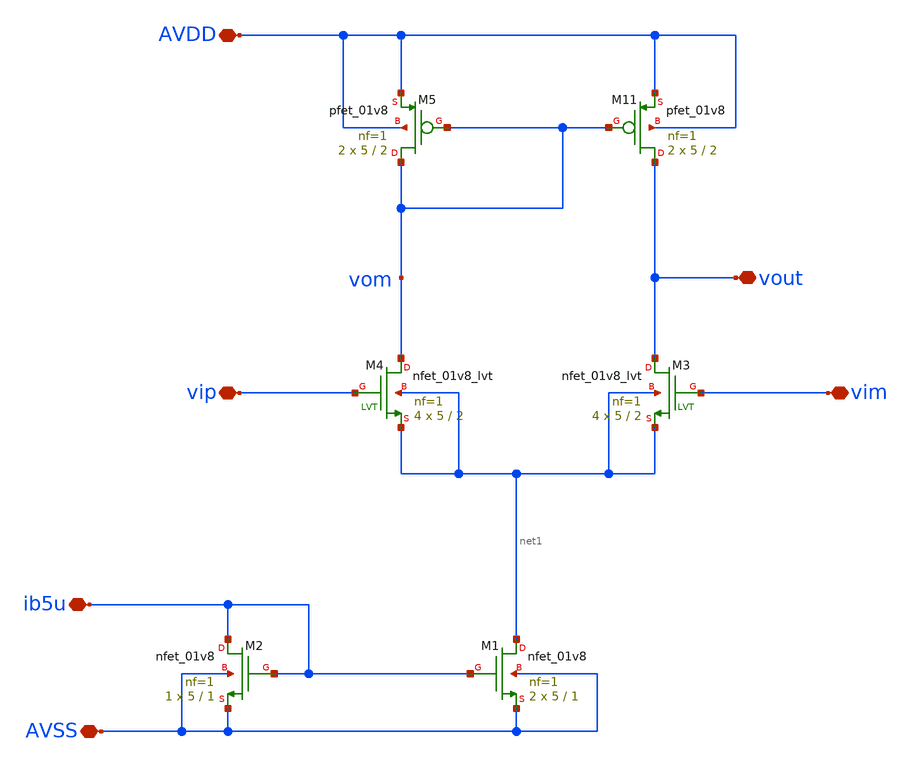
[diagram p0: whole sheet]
** sch_path: xschem/Opa_nmos1.sch
**.subckt Opa_nmos1 vip vim AVDD AVSS vout ib5u
*.iopin vip
*.iopin vim
*.iopin AVDD
*.iopin AVSS
*.iopin vout
*.iopin ib5u
XM4 vom vip net1 net1 sky130_fd_pr__nfet_01v8_lvt L=2 W=5 nf=1 ad='int((1 + 1)/2) * 5 / 1 * 0.29' as='int((1 + 2)/2) * 5 / 1 * 0.29'
+ pd='2*int((1 + 1)/2) * (5 / 1 + 0.29)' ps='2*int((1 + 2)/2) * (5 / 1 + 0.29)' nrd='0.29 / 5 ' nrs='0.29 / 5 '
+ sa=0 sb=0 sd=0 mult=4 m=4
XM11 vout vom AVDD AVDD sky130_fd_pr__pfet_01v8 L=2 W=5 nf=1 ad='int((nf+1)/2) * W/nf * 0.29' as='int((nf+2)/2) * W/nf * 0.29'
+ pd='2*int((nf+1)/2) * (W/nf + 0.29)' ps='2*int((nf+2)/2) * (W/nf + 0.29)' nrd='0.29 / W' nrs='0.29 / W'
+ sa=0 sb=0 sd=0 mult=2 m=2
XM2 ib5u ib5u AVSS AVSS sky130_fd_pr__nfet_01v8 L=1 W=5 nf=1 ad='int((1 + 1)/2) * 5 / 1 * 0.29' as='int((1 + 2)/2) * 5 / 1 * 0.29'
+ pd='2*int((1 + 1)/2) * (5 / 1 + 0.29)' ps='2*int((1 + 2)/2) * (5 / 1 + 0.29)' nrd='0.29 / 5 ' nrs='0.29 / 5 '
+ sa=0 sb=0 sd=0 mult=1 m=1
XM1 net1 ib5u AVSS AVSS sky130_fd_pr__nfet_01v8 L=1 W=5 nf=1 ad='int((1 + 1)/2) * 5 / 1 * 0.29' as='int((1 + 2)/2) * 5 / 1 * 0.29'
+ pd='2*int((1 + 1)/2) * (5 / 1 + 0.29)' ps='2*int((1 + 2)/2) * (5 / 1 + 0.29)' nrd='0.29 / 5 ' nrs='0.29 / 5 '
+ sa=0 sb=0 sd=0 mult=2 m=2
XM3 vout vim net1 net1 sky130_fd_pr__nfet_01v8_lvt L=2 W=5 nf=1 ad='int((1 + 1)/2) * 5 / 1 * 0.29' as='int((1 + 2)/2) * 5 / 1 * 0.29'
+ pd='2*int((1 + 1)/2) * (5 / 1 + 0.29)' ps='2*int((1 + 2)/2) * (5 / 1 + 0.29)' nrd='0.29 / 5 ' nrs='0.29 / 5 '
+ sa=0 sb=0 sd=0 mult=4 m=4
XM5 vom vom AVDD AVDD sky130_fd_pr__pfet_01v8 L=2 W=5 nf=1 ad='int((nf+1)/2) * W/nf * 0.29' as='int((nf+2)/2) * W/nf * 0.29'
+ pd='2*int((nf+1)/2) * (W/nf + 0.29)' ps='2*int((nf+2)/2) * (W/nf + 0.29)' nrd='0.29 / W' nrs='0.29 / W'
+ sa=0 sb=0 sd=0 mult=2 m=2
**.ends
.end
